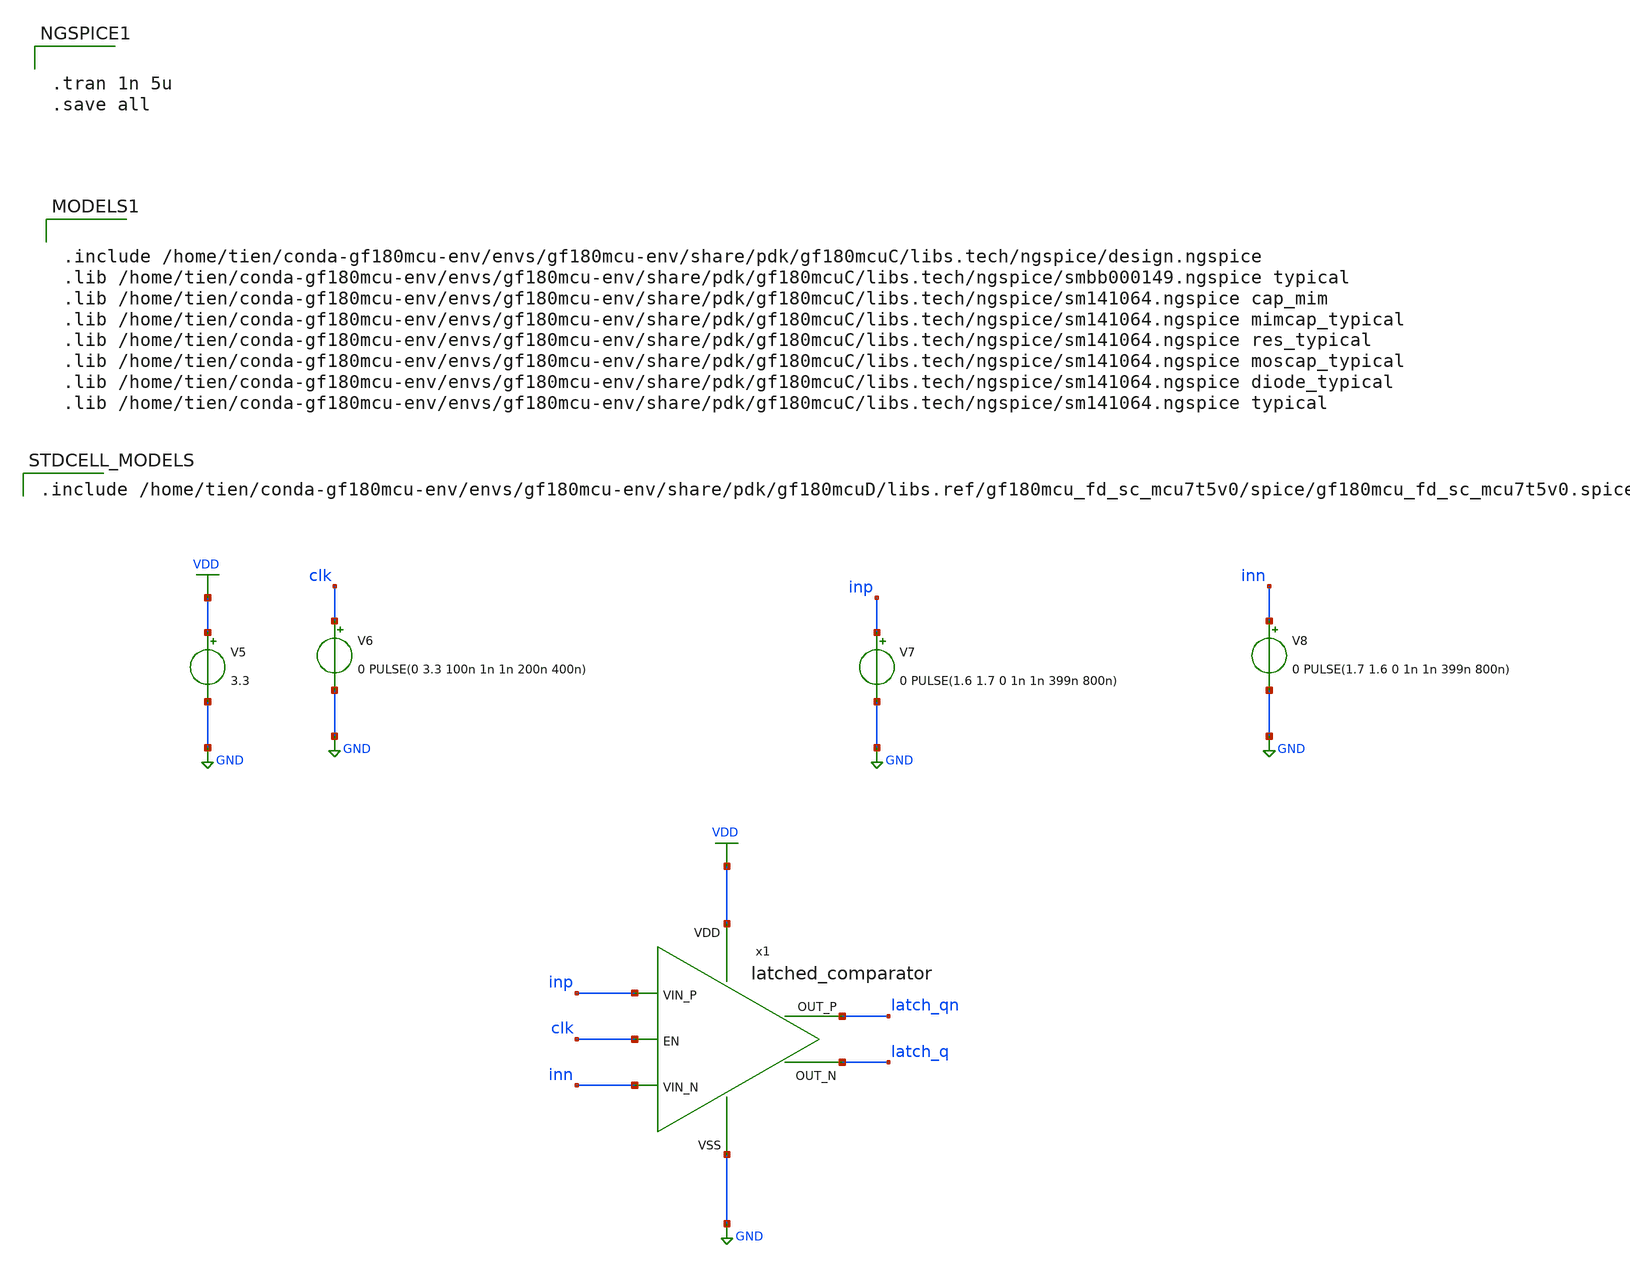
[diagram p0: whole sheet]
** sch_path: Schematic/comparator/latched_comparator_tb.sch
**.subckt latched_comparator_tb
x1 VDD inp inn clk latch_qn latch_q GND latched_comparator
V5 VDD GND 3.3
V6 clk GND 0 PULSE(0 3.3 100n 1n 1n 200n 400n)
V7 inp GND 0 PULSE(1.6 1.7 0 1n 1n 399n 800n)
V8 inn GND 0 PULSE(1.7 1.6 0 1n 1n 399n 800n)
**** begin user architecture code


.tran 1n 5u
.save all



.include /home/tien/conda-gf180mcu-env/envs/gf180mcu-env/share/pdk/gf180mcuC/libs.tech/ngspice/design.ngspice
.lib /home/tien/conda-gf180mcu-env/envs/gf180mcu-env/share/pdk/gf180mcuC/libs.tech/ngspice/smbb000149.ngspice typical
.lib /home/tien/conda-gf180mcu-env/envs/gf180mcu-env/share/pdk/gf180mcuC/libs.tech/ngspice/sm141064.ngspice cap_mim
.lib /home/tien/conda-gf180mcu-env/envs/gf180mcu-env/share/pdk/gf180mcuC/libs.tech/ngspice/sm141064.ngspice mimcap_typical
.lib /home/tien/conda-gf180mcu-env/envs/gf180mcu-env/share/pdk/gf180mcuC/libs.tech/ngspice/sm141064.ngspice res_typical
.lib /home/tien/conda-gf180mcu-env/envs/gf180mcu-env/share/pdk/gf180mcuC/libs.tech/ngspice/sm141064.ngspice moscap_typical
.lib /home/tien/conda-gf180mcu-env/envs/gf180mcu-env/share/pdk/gf180mcuC/libs.tech/ngspice/sm141064.ngspice diode_typical
.lib /home/tien/conda-gf180mcu-env/envs/gf180mcu-env/share/pdk/gf180mcuC/libs.tech/ngspice/sm141064.ngspice typical

 .include /home/tien/conda-gf180mcu-env/envs/gf180mcu-env/share/pdk/gf180mcuD/libs.ref/gf180mcu_fd_sc_mcu7t5v0/spice/gf180mcu_fd_sc_mcu7t5v0.spice
**** end user architecture code
**.ends
.GLOBAL VDD
.GLOBAL GND
.end
